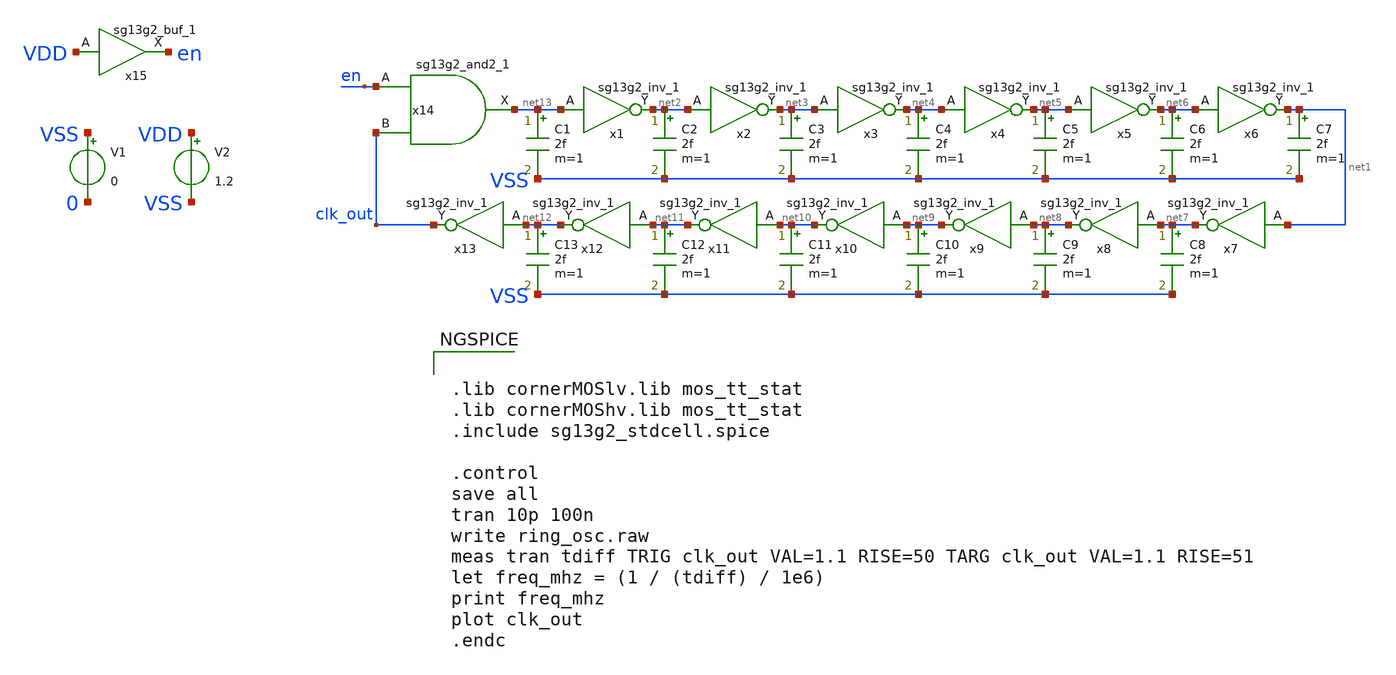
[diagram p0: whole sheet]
** sch_path: xschem/ring_osc.sch
* IHP-GmbH/IHP-Open-PDK/ihp-sg13g2/libs.tech/xschem/sg13g2_stdcells/sg13g2_buf_1.sch:
* Copyright 2023 IHP PDK Authors
* Licensed under the Apache License, Version 2.0 (the "License");
**.subckt ring_osc
x2 net3 net2 VDD VSS sg13g2_inv_1
x1 net2 net13 VDD VSS sg13g2_inv_1
x3 net4 net3 VDD VSS sg13g2_inv_1
x4 net5 net4 VDD VSS sg13g2_inv_1
x5 net6 net5 VDD VSS sg13g2_inv_1
x6 net1 net6 VDD VSS sg13g2_inv_1
x7 net7 net1 VDD VSS sg13g2_inv_1
x8 net8 net7 VDD VSS sg13g2_inv_1
x9 net9 net8 VDD VSS sg13g2_inv_1
x10 net10 net9 VDD VSS sg13g2_inv_1
x11 net11 net10 VDD VSS sg13g2_inv_1
x12 net12 net11 VDD VSS sg13g2_inv_1
x13 clk_out net12 VDD VSS sg13g2_inv_1
V1 VSS 0 0
V2 VDD VSS 1.2
C1 net13 VSS 2f m=1
C2 net2 VSS 2f m=1
C3 net3 VSS 2f m=1
C4 net4 VSS 2f m=1
C5 net5 VSS 2f m=1
C6 net6 VSS 2f m=1
C7 net1 VSS 2f m=1
C8 net7 VSS 2f m=1
C9 net8 VSS 2f m=1
C10 net9 VSS 2f m=1
C11 net10 VSS 2f m=1
C12 net11 VSS 2f m=1
C13 net12 VSS 2f m=1
x14 net13 en clk_out VDD VSS sg13g2_and2_1
x15 en VDD VDD VSS sg13g2_buf_1
**** begin user architecture code


.lib cornerMOSlv.lib mos_tt_stat
.lib cornerMOShv.lib mos_tt_stat
.include sg13g2_stdcell.spice

.control
save all
tran 10p 100n
write ring_osc.raw
meas tran tdiff TRIG clk_out VAL=1.1 RISE=50 TARG clk_out VAL=1.1 RISE=51
let freq_mhz = (1 / (tdiff) / 1e6)
print freq_mhz
plot clk_out
.endc


**** end user architecture code
**.ends

* expanding   symbol:  sg13g2_stdcells/sg13g2_inv_1.sym # of pins=2
** sym_path: sg13g2_stdcells/sg13g2_inv_1.sym
** sch_path: sg13g2_stdcells/sg13g2_inv_1.sch
.subckt sg13g2_inv_1 Y A VDD VSS
*.opin Y
*.ipin A
*.iopin VDD
*.iopin VSS
XM1 Y A VSS VSS sg13_lv_nmos w=740.00n l=130.00n ng=1 m=1 mm_ok=1
XM2 Y A VDD VDD sg13_lv_pmos w=1.12u l=130.00n ng=1 m=1 mm_ok=1
.ends


* expanding   symbol:  sg13g2_stdcells/sg13g2_and2_1.sym # of pins=3
** sym_path: sg13g2_stdcells/sg13g2_and2_1.sym
** sch_path: sg13g2_stdcells/sg13g2_and2_1.sch
.subckt sg13g2_and2_1 X A B VDD VSS
*.ipin A
*.ipin B
*.opin X
*.iopin VDD
*.iopin VSS
XM1 net1 A net2 VSS sg13_lv_nmos w=640.00n l=130.00n ng=1 m=1 mm_ok=1
XM2 net2 B VSS VSS sg13_lv_nmos w=640.00n l=130.00n ng=1 m=1 mm_ok=1
XM3 X net1 VSS VSS sg13_lv_nmos w=740.00n l=130.00n ng=1 m=1 mm_ok=1
XM4 net1 B VDD VDD sg13_lv_pmos w=840.00n l=130.00n ng=1 m=1 mm_ok=1
XM5 net1 A VDD VDD sg13_lv_pmos w=840.00n l=130.00n ng=1 m=1 mm_ok=1
XM6 X net1 VDD VDD sg13_lv_pmos w=1.12u l=130.00n ng=1 m=1 mm_ok=1
.ends


* expanding   symbol:  sg13g2_stdcells/sg13g2_buf_1.sym # of pins=2
** sym_path: sg13g2_stdcells/sg13g2_buf_1.sym
** sch_path: sg13g2_stdcells/sg13g2_buf_1.sch
.subckt sg13g2_buf_1 X A VDD VSS
*.ipin A
*.opin X
*.iopin VDD
*.iopin VSS
XM1 net1 A VSS VSS sg13_lv_nmos w=550.00n l=130.00n ng=1 m=1 mm_ok=1
XM2 X net1 VSS VSS sg13_lv_nmos w=740.00n l=130.00n ng=1 m=1 mm_ok=1
XM3 net1 A VDD VDD sg13_lv_pmos w=840.00n l=130.00n ng=1 m=1 mm_ok=1
XM4 X net1 VDD VDD sg13_lv_pmos w=1.12u l=130.00n ng=1 m=1 mm_ok=1
.ends

.end
